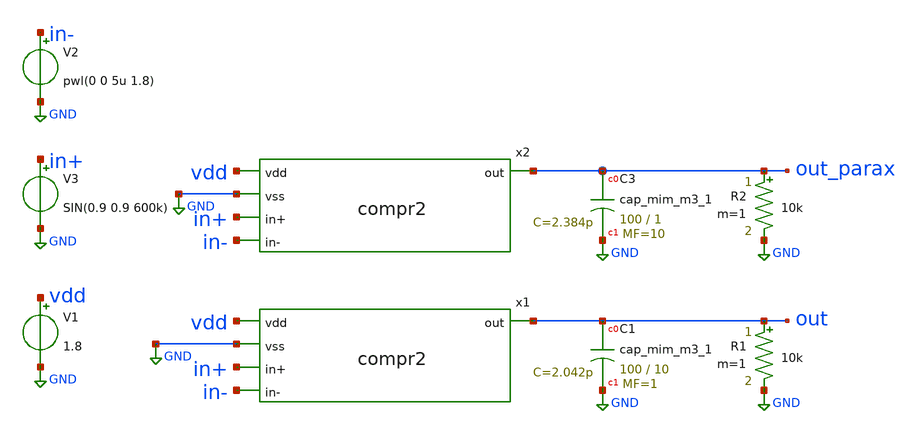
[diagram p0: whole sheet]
** sch_path: custom_gds/tt_um_tim2305_adc_dac/xschem/compr2_tb.sch
**.subckt compr2_tb
V1 vdd GND 1.8
V3 in+ GND SIN(0.9 0.9 600k)
V2 in- GND pwl(0 0 5u 1.8)
XC3 out_parax GND sky130_fd_pr__cap_mim_m3_1 W=100 L=1 MF=10 m=10
XC1 out GND sky130_fd_pr__cap_mim_m3_1 W=100 L=10 MF=1 m=1
R1 out GND 10k m=1
R2 out_parax GND 10k m=1
x1 vdd out GND in+ in- compr2
x2 vdd out_parax GND in+ in- compr2
**** begin user architecture code


.tran 100p 5u
.save all
.lib /home/ttuser/pdk/sky130A/libs.tech/ngspice/sky130.lib.spice tt


**** end user architecture code
**.ends

* expanding   symbol:  /home/ttuser/Documents/github_project/adc_dac2/xschem/compr2.sym # of pins=5
** sym_path: custom_gds/tt_um_tim2305_adc_dac/xschem/compr2.sym
** sch_path: custom_gds/tt_um_tim2305_adc_dac/xschem/compr2.sch
.subckt compr2 vdd out vss in+ in-
*.ipin in-
*.opin out
*.ipin in+
*.ipin vdd
*.ipin vss
XM1 vss net2 net2 vss sky130_fd_pr__nfet_01v8_lvt L=4 W=2 nf=1 ad='int((nf+1)/2) * W/nf * 0.29' as='int((nf+2)/2) * W/nf * 0.29'
+ pd='2*int((nf+1)/2) * (W/nf + 0.29)' ps='2*int((nf+2)/2) * (W/nf + 0.29)' nrd='0.29 / W' nrs='0.29 / W'
+ sa=0 sb=0 sd=0 mult=1 m=1
XM2 vss g1 g1 vss sky130_fd_pr__nfet_01v8_lvt L=4 W=2 nf=1 ad='int((nf+1)/2) * W/nf * 0.29' as='int((nf+2)/2) * W/nf * 0.29'
+ pd='2*int((nf+1)/2) * (W/nf + 0.29)' ps='2*int((nf+2)/2) * (W/nf + 0.29)' nrd='0.29 / W' nrs='0.29 / W'
+ sa=0 sb=0 sd=0 mult=1 m=1
XM3 vss net2 net4 vss sky130_fd_pr__nfet_01v8_lvt L=4 W=2 nf=1 ad='int((nf+1)/2) * W/nf * 0.29' as='int((nf+2)/2) * W/nf * 0.29'
+ pd='2*int((nf+1)/2) * (W/nf + 0.29)' ps='2*int((nf+2)/2) * (W/nf + 0.29)' nrd='0.29 / W' nrs='0.29 / W'
+ sa=0 sb=0 sd=0 mult=1 m=1
XM4 vss g1 net3 vss sky130_fd_pr__nfet_01v8_lvt L=4 W=2 nf=1 ad='int((nf+1)/2) * W/nf * 0.29' as='int((nf+2)/2) * W/nf * 0.29'
+ pd='2*int((nf+1)/2) * (W/nf + 0.29)' ps='2*int((nf+2)/2) * (W/nf + 0.29)' nrd='0.29 / W' nrs='0.29 / W'
+ sa=0 sb=0 sd=0 mult=1 m=1
XM5 net2 in+ net1 vdd sky130_fd_pr__pfet_01v8_lvt L=2 W=8 nf=1 ad='int((nf+1)/2) * W/nf * 0.29' as='int((nf+2)/2) * W/nf * 0.29'
+ pd='2*int((nf+1)/2) * (W/nf + 0.29)' ps='2*int((nf+2)/2) * (W/nf + 0.29)' nrd='0.29 / W' nrs='0.29 / W'
+ sa=0 sb=0 sd=0 mult=1 m=1
XM6 g1 in- net1 vdd sky130_fd_pr__pfet_01v8_lvt L=2 W=8 nf=1 ad='int((nf+1)/2) * W/nf * 0.29' as='int((nf+2)/2) * W/nf * 0.29'
+ pd='2*int((nf+1)/2) * (W/nf + 0.29)' ps='2*int((nf+2)/2) * (W/nf + 0.29)' nrd='0.29 / W' nrs='0.29 / W'
+ sa=0 sb=0 sd=0 mult=1 m=1
XM7 net4 net3 net5 vdd sky130_fd_pr__pfet_01v8_lvt L=4 W=4 nf=1 ad='int((nf+1)/2) * W/nf * 0.29' as='int((nf+2)/2) * W/nf * 0.29'
+ pd='2*int((nf+1)/2) * (W/nf + 0.29)' ps='2*int((nf+2)/2) * (W/nf + 0.29)' nrd='0.29 / W' nrs='0.29 / W'
+ sa=0 sb=0 sd=0 mult=1 m=1
XM9 net3 net3 net5 vdd sky130_fd_pr__pfet_01v8_lvt L=4 W=4 nf=1 ad='int((nf+1)/2) * W/nf * 0.29' as='int((nf+2)/2) * W/nf * 0.29'
+ pd='2*int((nf+1)/2) * (W/nf + 0.29)' ps='2*int((nf+2)/2) * (W/nf + 0.29)' nrd='0.29 / W' nrs='0.29 / W'
+ sa=0 sb=0 sd=0 mult=1 m=1
XM8 net1 vss vdd vdd sky130_fd_pr__pfet_01v8 L=8 W=2 nf=1 ad='int((nf+1)/2) * W/nf * 0.29' as='int((nf+2)/2) * W/nf * 0.29'
+ pd='2*int((nf+1)/2) * (W/nf + 0.29)' ps='2*int((nf+2)/2) * (W/nf + 0.29)' nrd='0.29 / W' nrs='0.29 / W'
+ sa=0 sb=0 sd=0 mult=1 m=1
XM10 net5 vss vdd vdd sky130_fd_pr__pfet_01v8 L=0.15 W=5 nf=1 ad='int((nf+1)/2) * W/nf * 0.29' as='int((nf+2)/2) * W/nf * 0.29'
+ pd='2*int((nf+1)/2) * (W/nf + 0.29)' ps='2*int((nf+2)/2) * (W/nf + 0.29)' nrd='0.29 / W' nrs='0.29 / W'
+ sa=0 sb=0 sd=0 mult=1 m=1
XM11 net6 net4 vdd vdd sky130_fd_pr__pfet_01v8 L=0.15 W=4 nf=1 ad='int((nf+1)/2) * W/nf * 0.29' as='int((nf+2)/2) * W/nf * 0.29'
+ pd='2*int((nf+1)/2) * (W/nf + 0.29)' ps='2*int((nf+2)/2) * (W/nf + 0.29)' nrd='0.29 / W' nrs='0.29 / W'
+ sa=0 sb=0 sd=0 mult=1 m=1
XM12 net6 net4 vss vss sky130_fd_pr__nfet_01v8 L=0.15 W=1 nf=1 ad='int((nf+1)/2) * W/nf * 0.29' as='int((nf+2)/2) * W/nf * 0.29'
+ pd='2*int((nf+1)/2) * (W/nf + 0.29)' ps='2*int((nf+2)/2) * (W/nf + 0.29)' nrd='0.29 / W' nrs='0.29 / W'
+ sa=0 sb=0 sd=0 mult=1 m=1
XM13 out net6 vdd vdd sky130_fd_pr__pfet_01v8 L=0.15 W=8 nf=1 ad='int((nf+1)/2) * W/nf * 0.29' as='int((nf+2)/2) * W/nf * 0.29'
+ pd='2*int((nf+1)/2) * (W/nf + 0.29)' ps='2*int((nf+2)/2) * (W/nf + 0.29)' nrd='0.29 / W' nrs='0.29 / W'
+ sa=0 sb=0 sd=0 mult=1 m=1
XM14 out net6 vss vss sky130_fd_pr__nfet_01v8 L=0.15 W=2 nf=1 ad='int((nf+1)/2) * W/nf * 0.29' as='int((nf+2)/2) * W/nf * 0.29'
+ pd='2*int((nf+1)/2) * (W/nf + 0.29)' ps='2*int((nf+2)/2) * (W/nf + 0.29)' nrd='0.29 / W' nrs='0.29 / W'
+ sa=0 sb=0 sd=0 mult=1 m=1
.ends

.GLOBAL GND
.end
